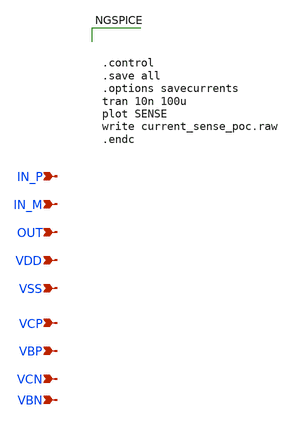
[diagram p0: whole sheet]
** sch_path: design/comparator/comparator_functional.sch
**.subckt comparator_functional IN_P IN_M OUT VDD VSS VCP VBP VCN VBN
*.ipin IN_P
*.ipin IN_M
*.ipin OUT
*.ipin VDD
*.ipin VSS
*.ipin VCP
*.ipin VBP
*.ipin VCN
*.ipin VBN
**** begin user architecture code



.control
.save all
.options savecurrents
tran 10n 100u
plot SENSE
write current_sense_poc.raw
.endc





.subckt uopamp_lvl2 +IN -IN VCC VEE OUT
* Universal Opamp Level 2
* Single pole opamp with rail saturation, current consumption, current limiting, and input offset
*+ voltage
*
* PINOUT ORDER  1   2   3   4   5
* PINOUT ORDER +IN -IN VCC VEE OUT
*
* Parameters:
* Avol => open-loop voltage gain (V/V), default=100k
* GBW => gain-bandwidth product (Hz), default=100meg
* Rin => differential input resistance (ohm), default=100g
* Rout => open-loop output resistance (ohm), default=1
* Iq => quiescent supply current (A), default=1m
* Ilimit => maximum output current (A), default=1
* Vrail => voltage between output saturation and each rail (V), default=0
* Vos => input offset voltage (V), default=0
* Vmax => total maximum supply voltage between rails (V), default=50
*
G1 VCC N001 N002 -IN 1u
G2 VEE N001 N002 -IN 1u
R1 VCC N001 {Avol/1u}
R2 N001 VEE {Avol/1u}
G3 OUT VCC VCC N001 {1/(2*Rout)}
G4 VEE OUT N001 VEE {1/(2*Rout)}
R4 VCC OUT {2*Rout}
R5 OUT VEE {2*Rout}
C1 VCC N001 {1u/(2*pi*GBW)}
C2 N001 VEE {1u/(2*pi*GBW)}
G6 N005 VEE N001 OUT {1/(2*Rout)}
G5 N006 VEE OUT N001 {1/(2*Rout)}
R8 -IN +IN {Rin}
V6 VCC N003 {Vrail+545m}
V7 N008 VEE {Vrail+545m}
V8 N002 +IN {Vos}
V9 OUT N007 {Ilimit-545m}
V10 N004 OUT {Ilimit-545m}
D1 N001 N003 diode
D2 N008 N001 diode
D3 VCC N005 diode
D4 VCC N006 diode
D5 VEE N005 zener
D6 VEE N006 zener
D7 N001 N004 diode
D8 N007 N001 diode
I1 VCC VEE {Iq}
.param Avol = 100k
.param GBW = 100meg
.param Rin = 100g
.param Rout = 1
.param Iq = 1m
.param Ilimit = 1
.param Vrail = 0
.param Vos = 0
.param Vmax = 50
.model diode D(Is=1e-14)
.model zener D(Is=1e-14 BV={Vmax})
.param pi=3.1415926535898
.ends

x10 IN_P IN_M VDD VSS OUT uopamp_lvl2


**** end user architecture code
**.ends
.end
